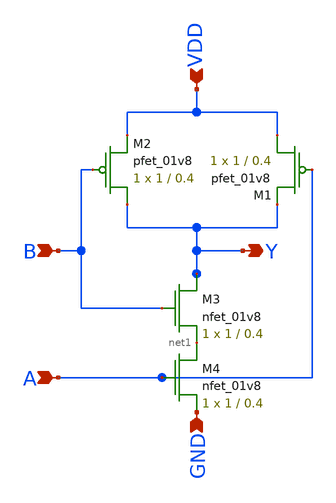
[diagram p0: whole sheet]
** sch_path: MP1/xschem/nand2.sch
**.subckt nand2 A B Y VDD GND
*.ipin A
*.ipin B
*.opin Y
*.ipin VDD
*.ipin GND
XM1 VDD A Y VDD sky130_fd_pr__pfet_01v8 L=0.4 W=1 nf=1 ad='int((nf+1)/2) * W/nf * 0.29' as='int((nf+2)/2) * W/nf * 0.29'
+ pd='2*int((nf+1)/2) * (W/nf + 0.29)' ps='2*int((nf+2)/2) * (W/nf + 0.29)' nrd='0.29 / W' nrs='0.29 / W'
+ sa=0 sb=0 sd=0 mult=1 m=1
XM2 Y B VDD VDD sky130_fd_pr__pfet_01v8 L=0.4 W=1 nf=1 ad='int((nf+1)/2) * W/nf * 0.29' as='int((nf+2)/2) * W/nf * 0.29'
+ pd='2*int((nf+1)/2) * (W/nf + 0.29)' ps='2*int((nf+2)/2) * (W/nf + 0.29)' nrd='0.29 / W' nrs='0.29 / W'
+ sa=0 sb=0 sd=0 mult=1 m=1
XM3 Y B net1 GND sky130_fd_pr__nfet_01v8 L=0.4 W=1 nf=1 ad='int((nf+1)/2) * W/nf * 0.29' as='int((nf+2)/2) * W/nf * 0.29'
+ pd='2*int((nf+1)/2) * (W/nf + 0.29)' ps='2*int((nf+2)/2) * (W/nf + 0.29)' nrd='0.29 / W' nrs='0.29 / W'
+ sa=0 sb=0 sd=0 mult=1 m=1
XM4 net1 A GND GND sky130_fd_pr__nfet_01v8 L=0.4 W=1 nf=1 ad='int((nf+1)/2) * W/nf * 0.29' as='int((nf+2)/2) * W/nf * 0.29'
+ pd='2*int((nf+1)/2) * (W/nf + 0.29)' ps='2*int((nf+2)/2) * (W/nf + 0.29)' nrd='0.29 / W' nrs='0.29 / W'
+ sa=0 sb=0 sd=0 mult=1 m=1
**.ends
.end
